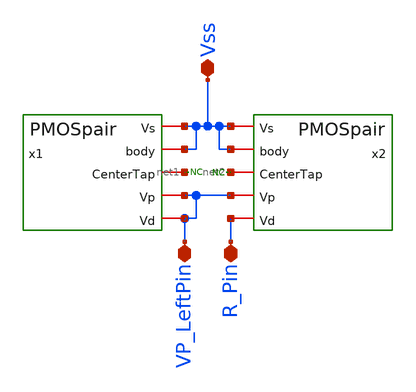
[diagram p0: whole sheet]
** sch_path: xschem/PrimalStructures/Level2/ConnectedPMOSPair.sch
**.subckt ConnectedPMOSPair Vss VP_LeftPin R_Pin
*.iopin Vss
*.iopin VP_LeftPin
*.iopin R_Pin
x1 Vss Vss net1 VP_LeftPin VP_LeftPin PMOSPair
x2 Vss Vss net2 VP_LeftPin R_Pin PMOSPair
* noconn #net2
* noconn #net1
**** begin user architecture code

** opencircuitdesign pdks install
.lib $::SKYWATER_MODELS/sky130.lib.spice tt


**** end user architecture code
**.ends

* expanding   symbol:  PrimalStructures/PMOSPair.sym # of pins=5
** sym_path: xschem/PrimalStructures/PMOSPair.sym
** sch_path: xschem/PrimalStructures/PMOSPair.sch
.subckt PMOSPair Vs body CenterTap Vp Vd
*.iopin Vp
*.iopin Vs
*.iopin body
*.iopin Vd
*.iopin CenterTap
XM7 Vd Vp CenterTap body sky130_fd_pr__pfet_g5v0d10v5 L=2 W=20 nf=1 ad='int((nf+1)/2) * W/nf * 0.29'
+ as='int((nf+2)/2) * W/nf * 0.29' pd='2*int((nf+1)/2) * (W/nf + 0.29)' ps='2*int((nf+2)/2) * (W/nf + 0.29)'
+ nrd='0.29 / W' nrs='0.29 / W' sa=0 sb=0 sd=0 mult=1 m=1
XM8 Vd Vp CenterTap body sky130_fd_pr__pfet_g5v0d10v5 L=2 W=20 nf=1 ad='int((nf+1)/2) * W/nf * 0.29'
+ as='int((nf+2)/2) * W/nf * 0.29' pd='2*int((nf+1)/2) * (W/nf + 0.29)' ps='2*int((nf+2)/2) * (W/nf + 0.29)'
+ nrd='0.29 / W' nrs='0.29 / W' sa=0 sb=0 sd=0 mult=1 m=1
XM9 Vd Vp CenterTap body sky130_fd_pr__pfet_g5v0d10v5 L=2 W=20 nf=1 ad='int((nf+1)/2) * W/nf * 0.29'
+ as='int((nf+2)/2) * W/nf * 0.29' pd='2*int((nf+1)/2) * (W/nf + 0.29)' ps='2*int((nf+2)/2) * (W/nf + 0.29)'
+ nrd='0.29 / W' nrs='0.29 / W' sa=0 sb=0 sd=0 mult=1 m=1
XM10 Vd Vp CenterTap body sky130_fd_pr__pfet_g5v0d10v5 L=2 W=20 nf=1 ad='int((nf+1)/2) * W/nf * 0.29'
+ as='int((nf+2)/2) * W/nf * 0.29' pd='2*int((nf+1)/2) * (W/nf + 0.29)' ps='2*int((nf+2)/2) * (W/nf + 0.29)'
+ nrd='0.29 / W' nrs='0.29 / W' sa=0 sb=0 sd=0 mult=1 m=1
XM11 Vd Vp CenterTap body sky130_fd_pr__pfet_g5v0d10v5 L=2 W=20 nf=1 ad='int((nf+1)/2) * W/nf * 0.29'
+ as='int((nf+2)/2) * W/nf * 0.29' pd='2*int((nf+1)/2) * (W/nf + 0.29)' ps='2*int((nf+2)/2) * (W/nf + 0.29)'
+ nrd='0.29 / W' nrs='0.29 / W' sa=0 sb=0 sd=0 mult=1 m=1
XM12 CenterTap Vp Vs body sky130_fd_pr__pfet_g5v0d10v5 L=5 W=30 nf=1 ad='int((nf+1)/2) * W/nf * 0.29'
+ as='int((nf+2)/2) * W/nf * 0.29' pd='2*int((nf+1)/2) * (W/nf + 0.29)' ps='2*int((nf+2)/2) * (W/nf + 0.29)'
+ nrd='0.29 / W' nrs='0.29 / W' sa=0 sb=0 sd=0 mult=1 m=1
.ends

.end
